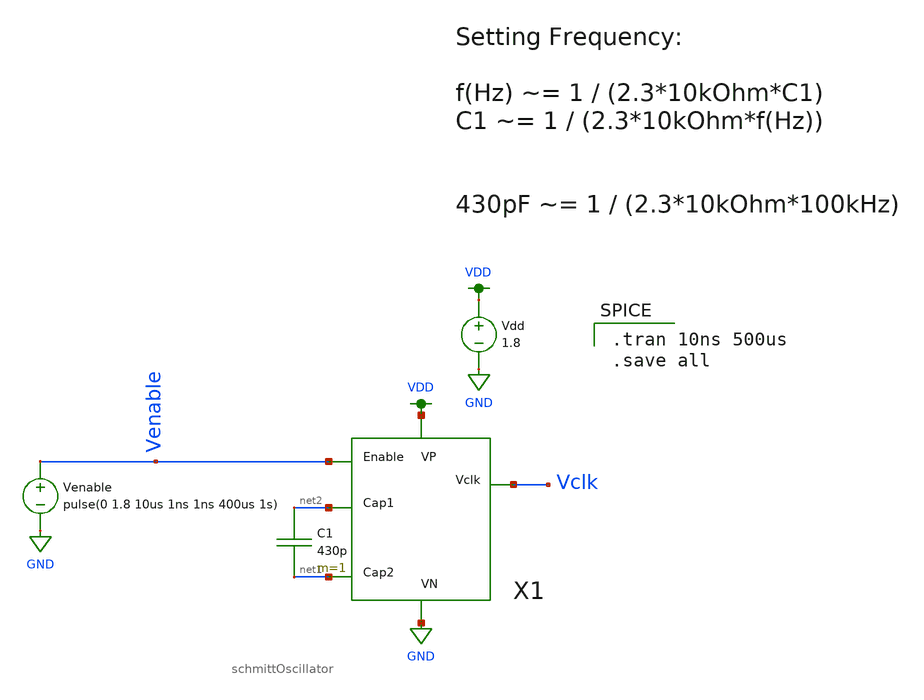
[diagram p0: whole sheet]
** sch_path: schematics/oscillatorTestbench.sch
**.subckt oscillatorTestbench
Vdd VDD GND 1.8
Venable Venable GND pulse(0 1.8 10us 1ns 1ns 400us 1s)
X1 Venable net2 net1 VDD GND Vclk schmittOscillator
C1 net2 net1 430p m=1
**** begin user architecture code

.option wnflag=1
.lib ~/skywater/skywater-pdk/libraries/sky130_fd_pr_ngspice/latest/models/sky130.lib.spice tt


.tran 10ns 500us
.save all

**** end user architecture code
**.ends

* expanding   symbol:  /home/madvlsi/Documents/final/xschem/schmittOscillator.sym # of pins=6
** sym_path: schematics/schmittOscillator.sym
** sch_path: schematics/schmittOscillator.sch
.subckt schmittOscillator Enable Cap1 Cap2 VP VN Vclk
*.ipin Enable
*.iopin Cap1
*.iopin Cap2
*.iopin VP
*.iopin VN
*.opin Vclk
**** begin user architecture code

.param l=.15
.param w=1
.param mL=4
.param mS=1
.param m=2
.param mp=2
.param mn=1

**** end user architecture code
X1 net1 VP VN net2 inverterSchmitt
X2 net2 VP VN Cap1 inverterSchmitt
X3 Cap1 VP VN net3 inverterSchmitt
R1 net3 Cap2 10k m=1
R2 Cap2 net4 100k m=1
X4 net3 VP VN net5 inverterSchmitt
X5 net5 VP VN Vclk inverterSchmitt
C3 Vclk VN 4p m=1
X6 Enable net4 VP VN net1 and
.ends


* expanding   symbol:  /home/madvlsi/Documents/final/xschem/inverterSchmitt.sym # of pins=4
** sym_path: schematics/inverterSchmitt.sym
** sch_path: schematics/inverterSchmitt.sch
.subckt inverterSchmitt A VP VN Z
*.ipin A
*.iopin VP
*.iopin VN
*.opin Z
XM1 net1 A VN GND sky130_fd_pr__nfet_01v8 L=l W=w nf=1 ad='int((nf+1)/2) * W/nf * 0.29' as='int((nf+2)/2) * W/nf * 0.29'
+ pd='2*int((nf+1)/2) * (W/nf + 0.29)' ps='2*int((nf+2)/2) * (W/nf + 0.29)' nrd='0.29 / W' nrs='0.29 / W'
+ sa=0 sb=0 sd=0 mult=m m=m
XM2 net1 A VP VDD sky130_fd_pr__pfet_01v8 L=l W=w nf=1 ad='int((nf+1)/2) * W/nf * 0.29' as='int((nf+2)/2) * W/nf * 0.29'
+ pd='2*int((nf+1)/2) * (W/nf + 0.29)' ps='2*int((nf+2)/2) * (W/nf + 0.29)' nrd='0.29 / W' nrs='0.29 / W'
+ sa=0 sb=0 sd=0 mult=mL m=mL
XM5 net2 net1 VP VDD sky130_fd_pr__pfet_01v8 L=l W=w nf=1 ad='int((nf+1)/2) * W/nf * 0.29' as='int((nf+2)/2) * W/nf * 0.29'
+ pd='2*int((nf+1)/2) * (W/nf + 0.29)' ps='2*int((nf+2)/2) * (W/nf + 0.29)' nrd='0.29 / W' nrs='0.29 / W'
+ sa=0 sb=0 sd=0 mult=mL m=mL
XM6 net2 net1 VN GND sky130_fd_pr__nfet_01v8 L=l W=w nf=1 ad='int((nf+1)/2) * W/nf * 0.29' as='int((nf+2)/2) * W/nf * 0.29'
+ pd='2*int((nf+1)/2) * (W/nf + 0.29)' ps='2*int((nf+2)/2) * (W/nf + 0.29)' nrd='0.29 / W' nrs='0.29 / W'
+ sa=0 sb=0 sd=0 mult=m m=m
XM3 VP net2 net1 VP sky130_fd_pr__pfet_01v8 L=l W=w nf=1 ad='int((nf+1)/2) * W/nf * 0.29' as='int((nf+2)/2) * W/nf * 0.29'
+ pd='2*int((nf+1)/2) * (W/nf + 0.29)' ps='2*int((nf+2)/2) * (W/nf + 0.29)' nrd='0.29 / W' nrs='0.29 / W'
+ sa=0 sb=0 sd=0 mult=m m=m
XM4 VN net2 net1 VN sky130_fd_pr__nfet_01v8 L=l W=w nf=1 ad='int((nf+1)/2) * W/nf * 0.29' as='int((nf+2)/2) * W/nf * 0.29'
+ pd='2*int((nf+1)/2) * (W/nf + 0.29)' ps='2*int((nf+2)/2) * (W/nf + 0.29)' nrd='0.29 / W' nrs='0.29 / W'
+ sa=0 sb=0 sd=0 mult=mS m=mS
XM7 Z net2 VP VDD sky130_fd_pr__pfet_01v8 L=l W=w nf=1 ad='int((nf+1)/2) * W/nf * 0.29' as='int((nf+2)/2) * W/nf * 0.29'
+ pd='2*int((nf+1)/2) * (W/nf + 0.29)' ps='2*int((nf+2)/2) * (W/nf + 0.29)' nrd='0.29 / W' nrs='0.29 / W'
+ sa=0 sb=0 sd=0 mult=mL m=mL
XM8 Z net2 VN GND sky130_fd_pr__nfet_01v8 L=l W=w nf=1 ad='int((nf+1)/2) * W/nf * 0.29' as='int((nf+2)/2) * W/nf * 0.29'
+ pd='2*int((nf+1)/2) * (W/nf + 0.29)' ps='2*int((nf+2)/2) * (W/nf + 0.29)' nrd='0.29 / W' nrs='0.29 / W'
+ sa=0 sb=0 sd=0 mult=m m=m
**** begin user architecture code

.param l=.15
.param w=1
.param mL=4
.param mS=1
.param m=2

**** end user architecture code
.ends


* expanding   symbol:  /home/madvlsi/Documents/final/xschem/and.sym # of pins=6
** sym_path: schematics/and.sym
** sch_path: schematics/and.sch
.subckt and A B VP VN Z
*.ipin A
*.ipin B
*.iopin VP
*.iopin VN
*.opin Z
X1 net1 VP VN Z inverter
X2 A B VP VN net1 nand
**** begin user architecture code

.param l=.15
.param w=1
.param mn=1
.param mp=1

**** end user architecture code
.ends


* expanding   symbol:  /home/madvlsi/Documents/final/xschem/inverter.sym # of pins=4
** sym_path: schematics/inverter.sym
** sch_path: schematics/inverter.sch
.subckt inverter A VP VN Z
*.ipin A
*.iopin VP
*.iopin VN
*.opin Z
XM1 Z A VN GND sky130_fd_pr__nfet_01v8 L=l W=w nf=1 ad='int((nf+1)/2) * W/nf * 0.29' as='int((nf+2)/2) * W/nf * 0.29'
+ pd='2*int((nf+1)/2) * (W/nf + 0.29)' ps='2*int((nf+2)/2) * (W/nf + 0.29)' nrd='0.29 / W' nrs='0.29 / W'
+ sa=0 sb=0 sd=0 mult=mn m=mn
XM2 Z A VP VDD sky130_fd_pr__pfet_01v8 L=l W=w nf=1 ad='int((nf+1)/2) * W/nf * 0.29' as='int((nf+2)/2) * W/nf * 0.29'
+ pd='2*int((nf+1)/2) * (W/nf + 0.29)' ps='2*int((nf+2)/2) * (W/nf + 0.29)' nrd='0.29 / W' nrs='0.29 / W'
+ sa=0 sb=0 sd=0 mult=mp m=mp
**** begin user architecture code

.param l=.15
.param w=1
.param mn=1
.param mp=1

**** end user architecture code
.ends


* expanding   symbol:  /home/madvlsi/Documents/final/xschem/nand.sym # of pins=6
** sym_path: schematics/nand.sym
** sch_path: schematics/nand.sch
.subckt nand A B VP VN Z
*.ipin A
*.iopin VP
*.iopin VN
*.opin Z
*.ipin B
XM1 Z A net1 GND sky130_fd_pr__nfet_01v8 L=0.15 W=1 nf=1 ad='int((nf+1)/2) * W/nf * 0.29' as='int((nf+2)/2) * W/nf * 0.29'
+ pd='2*int((nf+1)/2) * (W/nf + 0.29)' ps='2*int((nf+2)/2) * (W/nf + 0.29)' nrd='0.29 / W' nrs='0.29 / W'
+ sa=0 sb=0 sd=0 mult=1 m=1
XM2 VP B Z VDD sky130_fd_pr__pfet_01v8 L=0.15 W=1 nf=1 ad='int((nf+1)/2) * W/nf * 0.29' as='int((nf+2)/2) * W/nf * 0.29'
+ pd='2*int((nf+1)/2) * (W/nf + 0.29)' ps='2*int((nf+2)/2) * (W/nf + 0.29)' nrd='0.29 / W' nrs='0.29 / W'
+ sa=0 sb=0 sd=0 mult=2 m=2
XM3 VN B net1 GND sky130_fd_pr__nfet_01v8 L=0.15 W=1 nf=1 ad='int((nf+1)/2) * W/nf * 0.29' as='int((nf+2)/2) * W/nf * 0.29'
+ pd='2*int((nf+1)/2) * (W/nf + 0.29)' ps='2*int((nf+2)/2) * (W/nf + 0.29)' nrd='0.29 / W' nrs='0.29 / W'
+ sa=0 sb=0 sd=0 mult=1 m=1
XM4 Z A VP VDD sky130_fd_pr__pfet_01v8 L=0.15 W=1 nf=1 ad='int((nf+1)/2) * W/nf * 0.29' as='int((nf+2)/2) * W/nf * 0.29'
+ pd='2*int((nf+1)/2) * (W/nf + 0.29)' ps='2*int((nf+2)/2) * (W/nf + 0.29)' nrd='0.29 / W' nrs='0.29 / W'
+ sa=0 sb=0 sd=0 mult=2 m=2
.ends

.GLOBAL GND
.GLOBAL VDD
.end
